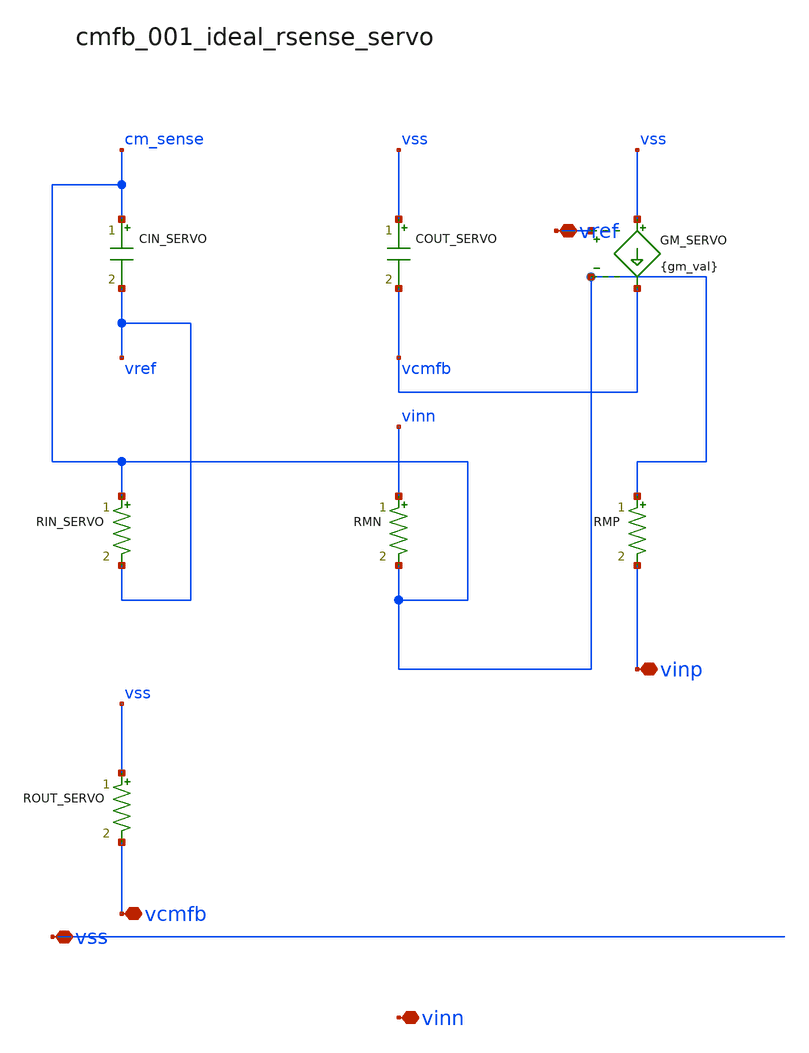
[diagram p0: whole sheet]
** sch_path: analog-db/raw/cmfb_001_ideal_rsense_servo/cmfb_001_ideal_rsense_servo_annotated.sch
**.subckt cmfb_001_ideal_rsense_servo_annotated vss vref vcmfb vinp vinn
*.iopin vss
*.iopin vref
*.iopin vcmfb
*.iopin vinp
*.iopin vinn
CIN_SERVO cm_sense vref 'cin_val' m=1
COUT_SERVO vss vcmfb 'cout_val' m=1
GM_SERVO vss vcmfb vref cm_sense {gm_val}
RIN_SERVO cm_sense vref 'rin_val' m=1
RMN vinn cm_sense 'x_dut_rmn_value' m=1
RMP cm_sense vinp 'x_dut_rmp_value' m=1
ROUT_SERVO vss vcmfb 'rout_val' m=1
**.ends
.end
